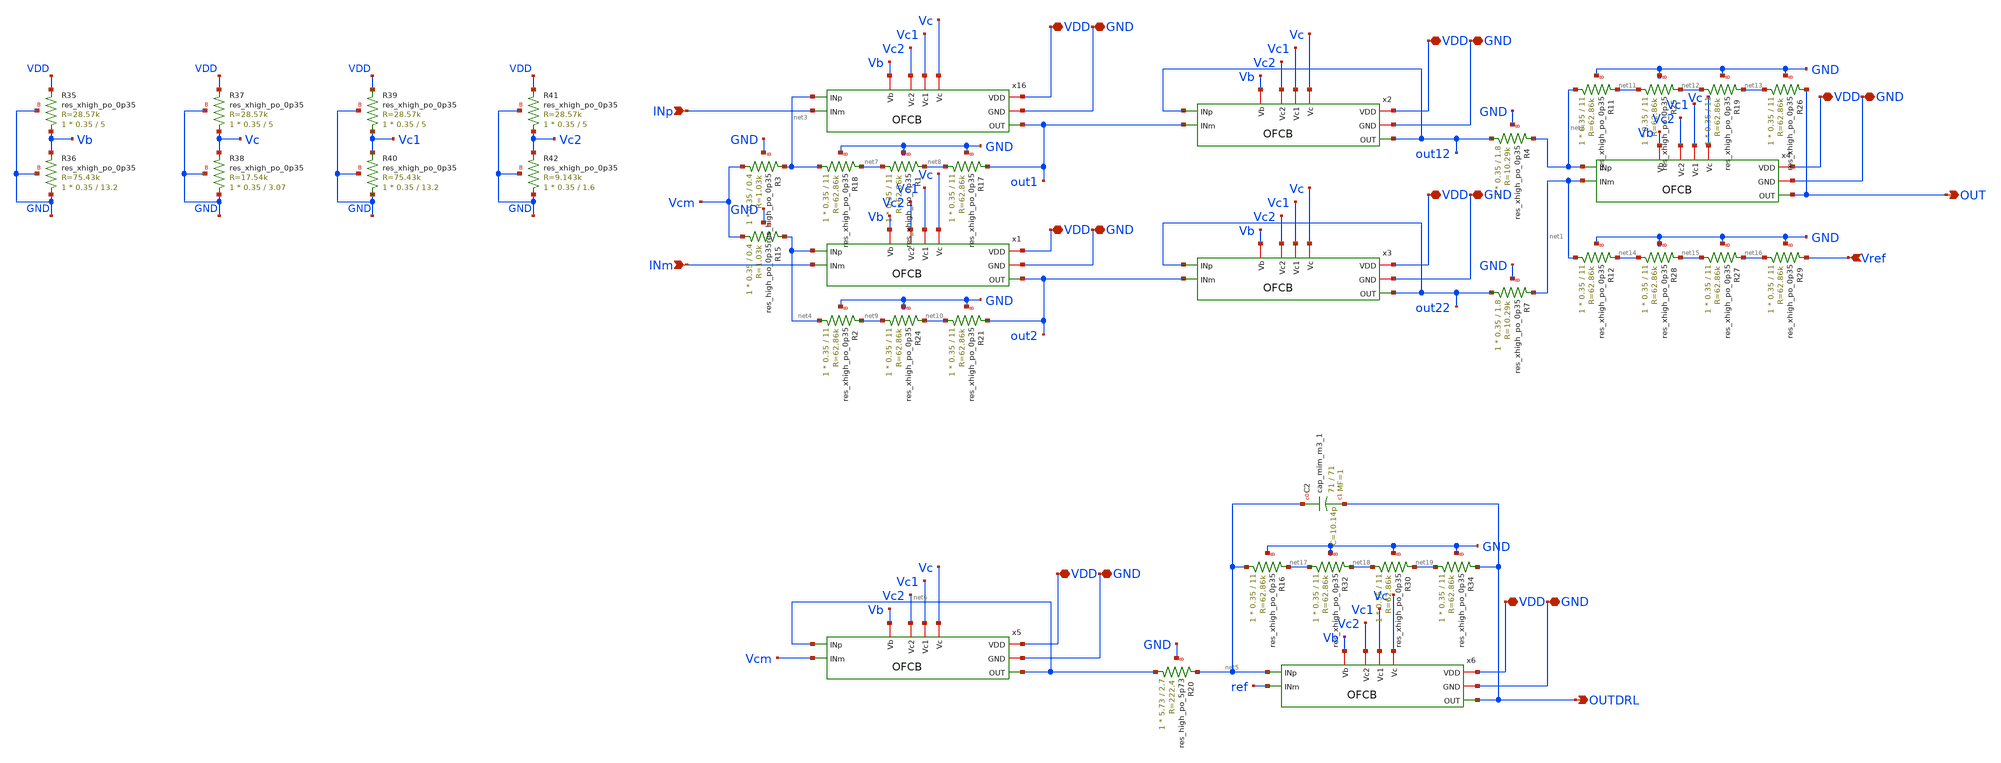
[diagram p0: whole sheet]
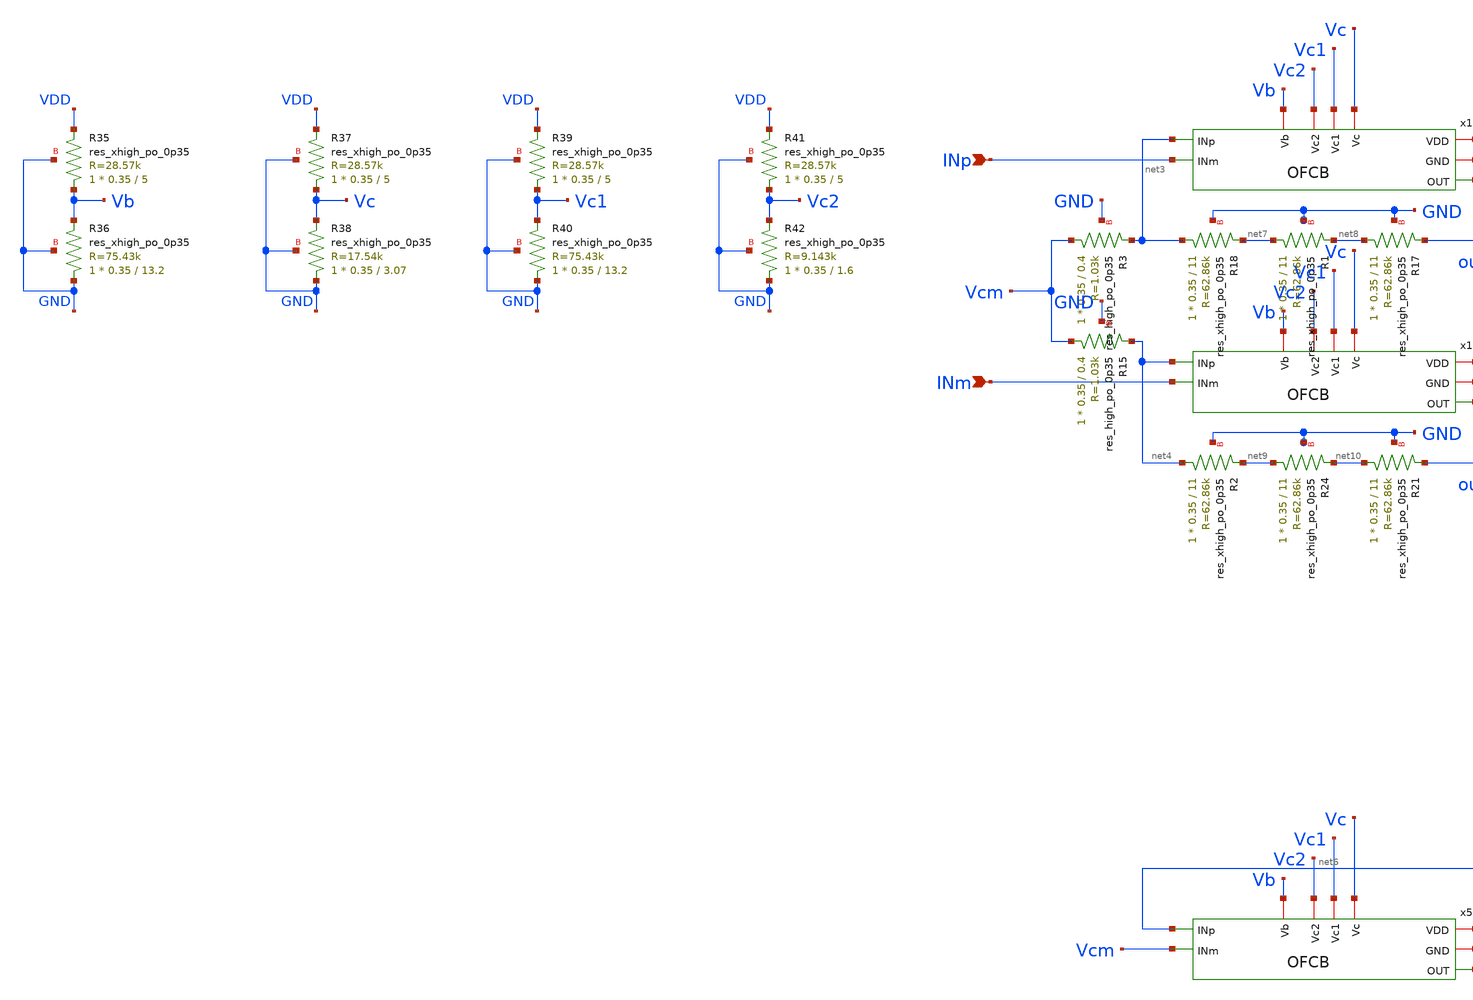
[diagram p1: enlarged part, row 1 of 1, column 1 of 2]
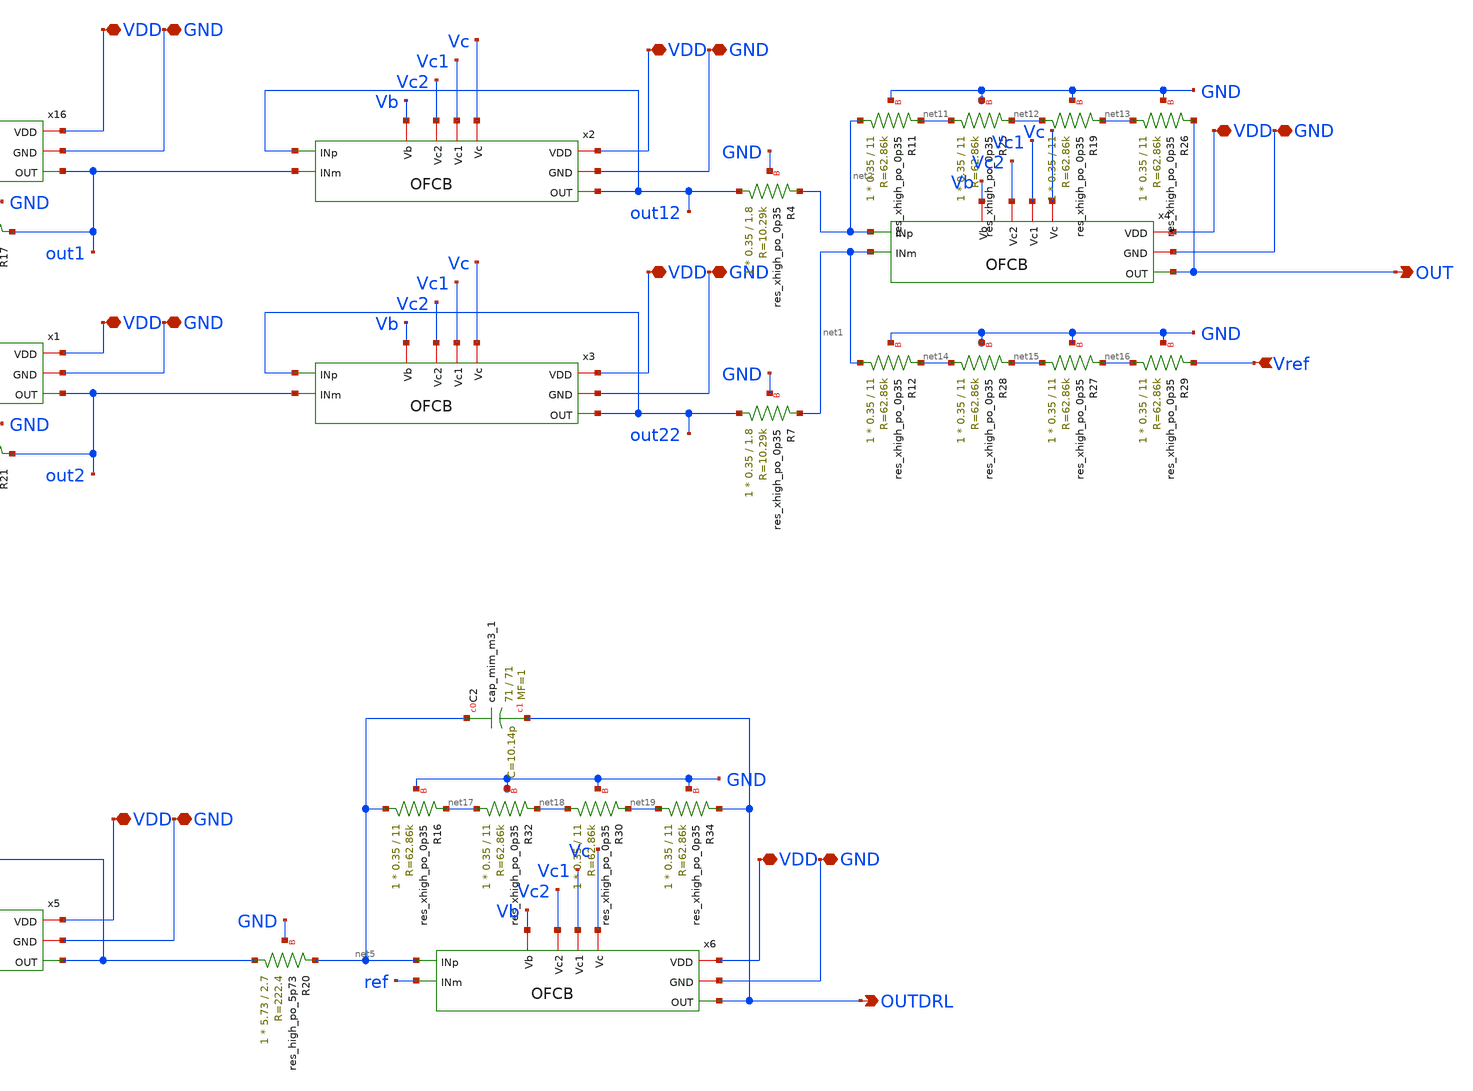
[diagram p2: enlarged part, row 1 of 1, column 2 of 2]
** sch_path: xschem/ecg.sch
**.subckt ecg VDD VDD GND GND VDD GND VDD GND VDD GND VDD GND VDD GND INp INm OUT Vref OUTDRL
*.iopin VDD
*.iopin VDD
*.iopin GND
*.iopin GND
*.iopin VDD
*.iopin GND
*.iopin VDD
*.iopin GND
*.iopin VDD
*.iopin GND
*.iopin VDD
*.iopin GND
*.iopin VDD
*.iopin GND
*.ipin INp
*.ipin INm
*.opin OUT
*.ipin Vref
*.opin OUTDRL
XR3 Vcm net3 GND sky130_fd_pr__res_high_po_0p35 L=0.4 mult=1 m=1
XR15 Vcm net4 GND sky130_fd_pr__res_high_po_0p35 L=0.4 mult=1 m=1
XR18 net3 net7 GND sky130_fd_pr__res_xhigh_po_0p35 L=11 mult=1 m=1
XR20 net6 net5 GND sky130_fd_pr__res_high_po_5p73 L=2.7 mult=1 m=1
XR17 net8 out1 GND sky130_fd_pr__res_xhigh_po_0p35 L=11 mult=1 m=1
XR1 net7 net8 GND sky130_fd_pr__res_xhigh_po_0p35 L=11 mult=1 m=1
XR2 net4 net9 GND sky130_fd_pr__res_xhigh_po_0p35 L=11 mult=1 m=1
XR21 net10 out2 GND sky130_fd_pr__res_xhigh_po_0p35 L=11 mult=1 m=1
XR24 net9 net10 GND sky130_fd_pr__res_xhigh_po_0p35 L=11 mult=1 m=1
XR4 out12 net2 GND sky130_fd_pr__res_xhigh_po_0p35 L=1.8 mult=1 m=1
XR7 out22 net1 GND sky130_fd_pr__res_xhigh_po_0p35 L=1.8 mult=1 m=1
XR11 net2 net11 GND sky130_fd_pr__res_xhigh_po_0p35 L=11 mult=1 m=1
XR19 net12 net13 GND sky130_fd_pr__res_xhigh_po_0p35 L=11 mult=1 m=1
XR25 net11 net12 GND sky130_fd_pr__res_xhigh_po_0p35 L=11 mult=1 m=1
XR26 net13 OUT GND sky130_fd_pr__res_xhigh_po_0p35 L=11 mult=1 m=1
XR12 net1 net14 GND sky130_fd_pr__res_xhigh_po_0p35 L=11 mult=1 m=1
XR27 net15 net16 GND sky130_fd_pr__res_xhigh_po_0p35 L=11 mult=1 m=1
XR28 net14 net15 GND sky130_fd_pr__res_xhigh_po_0p35 L=11 mult=1 m=1
XR29 net16 Vref GND sky130_fd_pr__res_xhigh_po_0p35 L=11 mult=1 m=1
XC2 net5 OUTDRL sky130_fd_pr__cap_mim_m3_1 W=71 L=71 MF=1 m=1
XR16 net5 net17 GND sky130_fd_pr__res_xhigh_po_0p35 L=11 mult=1 m=1
XR30 net18 net19 GND sky130_fd_pr__res_xhigh_po_0p35 L=11 mult=1 m=1
XR32 net17 net18 GND sky130_fd_pr__res_xhigh_po_0p35 L=11 mult=1 m=1
XR34 net19 OUTDRL GND sky130_fd_pr__res_xhigh_po_0p35 L=11 mult=1 m=1
x16 Vb VDD GND Vc2 out1 net3 INp Vc1 Vc OFCB
x1 Vb VDD GND Vc2 out2 net4 INm Vc1 Vc OFCB
x2 Vb VDD GND Vc2 out12 out12 out1 Vc1 Vc OFCB
x3 Vb VDD GND Vc2 out22 out22 out2 Vc1 Vc OFCB
x4 Vb VDD GND Vc2 OUT net2 net1 Vc1 Vc OFCB
x5 Vb VDD GND Vc2 net6 net6 Vcm Vc1 Vc OFCB
x6 Vb VDD GND Vc2 OUTDRL net5 ref Vc1 Vc OFCB
XR35 Vb VDD GND sky130_fd_pr__res_xhigh_po_0p35 L=5 mult=1 m=1
XR36 GND Vb GND sky130_fd_pr__res_xhigh_po_0p35 L=13.2 mult=1 m=1
XR37 Vc VDD GND sky130_fd_pr__res_xhigh_po_0p35 L=5 mult=1 m=1
XR38 GND Vc GND sky130_fd_pr__res_xhigh_po_0p35 L=3.07 mult=1 m=1
XR39 Vc1 VDD GND sky130_fd_pr__res_xhigh_po_0p35 L=5 mult=1 m=1
XR40 GND Vc1 GND sky130_fd_pr__res_xhigh_po_0p35 L=13.2 mult=1 m=1
XR41 Vc2 VDD GND sky130_fd_pr__res_xhigh_po_0p35 L=5 mult=1 m=1
XR42 GND Vc2 GND sky130_fd_pr__res_xhigh_po_0p35 L=1.6 mult=1 m=1
**.ends

* expanding   symbol:  OFCB.sym # of pins=9
** sym_path: xschem/OFCB.sym
** sch_path: xschem/OFCB.sch
.subckt OFCB Vb VDD GND Vc2 OUT INp INm Vc1 Vc
*.iopin VDD
*.iopin GND
*.opin OUT
*.ipin INp
*.ipin INm
*.iopin Vc2
*.iopin Vc1
*.iopin Vc
*.iopin Vb
XM11 S Vb VDD VDD sky130_fd_pr__pfet_01v8_lvt L=1 W=60 nf=1 ad='int((nf+1)/2) * W/nf * 0.29' as='int((nf+2)/2) * W/nf * 0.29'
+ pd='2*int((nf+1)/2) * (W/nf + 0.29)' ps='2*int((nf+2)/2) * (W/nf + 0.29)' nrd='0.29 / W' nrs='0.29 / W'
+ sa=0 sb=0 sd=0 mult=2 m=2
XM1 D1 INp S S sky130_fd_pr__pfet_01v8_lvt L=10 W=25 nf=2 ad='int((nf+1)/2) * W/nf * 0.29' as='int((nf+2)/2) * W/nf * 0.29'
+ pd='2*int((nf+1)/2) * (W/nf + 0.29)' ps='2*int((nf+2)/2) * (W/nf + 0.29)' nrd='0.29 / W' nrs='0.29 / W'
+ sa=0 sb=0 sd=0 mult=2 m=2
XM2 D2 INm S S sky130_fd_pr__pfet_01v8_lvt L=10 W=25 nf=2 ad='int((nf+1)/2) * W/nf * 0.29' as='int((nf+2)/2) * W/nf * 0.29'
+ pd='2*int((nf+1)/2) * (W/nf + 0.29)' ps='2*int((nf+2)/2) * (W/nf + 0.29)' nrd='0.29 / W' nrs='0.29 / W'
+ sa=0 sb=0 sd=0 mult=2 m=2
XM3 OUT Vc1 D2 GND sky130_fd_pr__nfet_01v8_lvt L=1 W=4 nf=1 ad='int((nf+1)/2) * W/nf * 0.29' as='int((nf+2)/2) * W/nf * 0.29'
+ pd='2*int((nf+1)/2) * (W/nf + 0.29)' ps='2*int((nf+2)/2) * (W/nf + 0.29)' nrd='0.29 / W' nrs='0.29 / W'
+ sa=0 sb=0 sd=0 mult=1 m=1
XM4 D2 Vc GND GND sky130_fd_pr__nfet_01v8_lvt L=1 W=2.8 nf=1 ad='int((nf+1)/2) * W/nf * 0.29' as='int((nf+2)/2) * W/nf * 0.29'
+ pd='2*int((nf+1)/2) * (W/nf + 0.29)' ps='2*int((nf+2)/2) * (W/nf + 0.29)' nrd='0.29 / W' nrs='0.29 / W'
+ sa=0 sb=0 sd=0 mult=1 m=1
XM5 D1 Vc GND GND sky130_fd_pr__nfet_01v8_lvt L=1 W=2.8 nf=1 ad='int((nf+1)/2) * W/nf * 0.29' as='int((nf+2)/2) * W/nf * 0.29'
+ pd='2*int((nf+1)/2) * (W/nf + 0.29)' ps='2*int((nf+2)/2) * (W/nf + 0.29)' nrd='0.29 / W' nrs='0.29 / W'
+ sa=0 sb=0 sd=0 mult=1 m=1
XM6 G Vc1 D1 GND sky130_fd_pr__nfet_01v8_lvt L=1 W=4 nf=1 ad='int((nf+1)/2) * W/nf * 0.29' as='int((nf+2)/2) * W/nf * 0.29'
+ pd='2*int((nf+1)/2) * (W/nf + 0.29)' ps='2*int((nf+2)/2) * (W/nf + 0.29)' nrd='0.29 / W' nrs='0.29 / W'
+ sa=0 sb=0 sd=0 mult=1 m=1
XM7 G Vc2 D9 D9 sky130_fd_pr__pfet_01v8_lvt L=2.23 W=5 nf=1 ad='int((nf+1)/2) * W/nf * 0.29' as='int((nf+2)/2) * W/nf * 0.29'
+ pd='2*int((nf+1)/2) * (W/nf + 0.29)' ps='2*int((nf+2)/2) * (W/nf + 0.29)' nrd='0.29 / W' nrs='0.29 / W'
+ sa=0 sb=0 sd=0 mult=1 m=1
XM9 D9 G VDD VDD sky130_fd_pr__pfet_01v8_lvt L=2.23 W=3.8 nf=1 ad='int((nf+1)/2) * W/nf * 0.29' as='int((nf+2)/2) * W/nf * 0.29'
+ pd='2*int((nf+1)/2) * (W/nf + 0.29)' ps='2*int((nf+2)/2) * (W/nf + 0.29)' nrd='0.29 / W' nrs='0.29 / W'
+ sa=0 sb=0 sd=0 mult=1 m=1
XM8 D10 G VDD VDD sky130_fd_pr__pfet_01v8_lvt L=2.23 W=3.8 nf=1 ad='int((nf+1)/2) * W/nf * 0.29' as='int((nf+2)/2) * W/nf * 0.29'
+ pd='2*int((nf+1)/2) * (W/nf + 0.29)' ps='2*int((nf+2)/2) * (W/nf + 0.29)' nrd='0.29 / W' nrs='0.29 / W'
+ sa=0 sb=0 sd=0 mult=1 m=1
XM10 OUT Vc2 D10 D10 sky130_fd_pr__pfet_01v8_lvt L=2.23 W=5 nf=1 ad='int((nf+1)/2) * W/nf * 0.29' as='int((nf+2)/2) * W/nf * 0.29'
+ pd='2*int((nf+1)/2) * (W/nf + 0.29)' ps='2*int((nf+2)/2) * (W/nf + 0.29)' nrd='0.29 / W' nrs='0.29 / W'
+ sa=0 sb=0 sd=0 mult=1 m=1
XC1 OUT D1 sky130_fd_pr__cap_mim_m3_1 W=50 L=20 MF=1 m=1
.ends

.end
